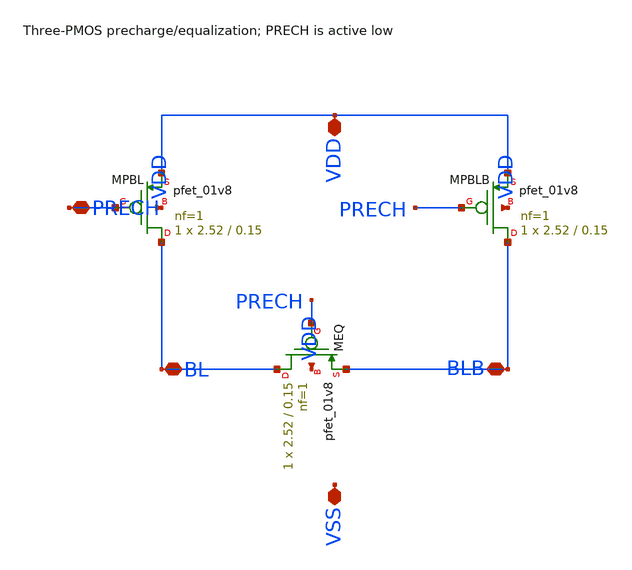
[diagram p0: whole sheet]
** sch_path: release/phase1/cells/precharge/precharge.sch
**.subckt precharge VDD BL BLB PRECH VSS
*.iopin VDD
*.iopin BL
*.iopin BLB
*.iopin PRECH
*.iopin VSS
XMPBL BL PRECH VDD VDD sky130_fd_pr__pfet_01v8 L=0.15 W=2.52 nf=1 ad='int((nf+1)/2) * W/nf * 0.29' as='int((nf+2)/2) * W/nf * 0.29'
+ pd='2*int((nf+1)/2) * (W/nf + 0.29)' ps='2*int((nf+2)/2) * (W/nf + 0.29)' nrd='0.29 / W' nrs='0.29 / W'
+ sa=0 sb=0 sd=0 mult=1 m=1
XMPBLB BLB PRECH VDD VDD sky130_fd_pr__pfet_01v8 L=0.15 W=2.52 nf=1 ad='int((nf+1)/2) * W/nf * 0.29'
+ as='int((nf+2)/2) * W/nf * 0.29' pd='2*int((nf+1)/2) * (W/nf + 0.29)' ps='2*int((nf+2)/2) * (W/nf + 0.29)'
+ nrd='0.29 / W' nrs='0.29 / W' sa=0 sb=0 sd=0 mult=1 m=1
XMEQ BL PRECH BLB VDD sky130_fd_pr__pfet_01v8 L=0.15 W=2.52 nf=1 ad='int((nf+1)/2) * W/nf * 0.29' as='int((nf+2)/2) * W/nf * 0.29'
+ pd='2*int((nf+1)/2) * (W/nf + 0.29)' ps='2*int((nf+2)/2) * (W/nf + 0.29)' nrd='0.29 / W' nrs='0.29 / W'
+ sa=0 sb=0 sd=0 mult=1 m=1
**.ends
.end
